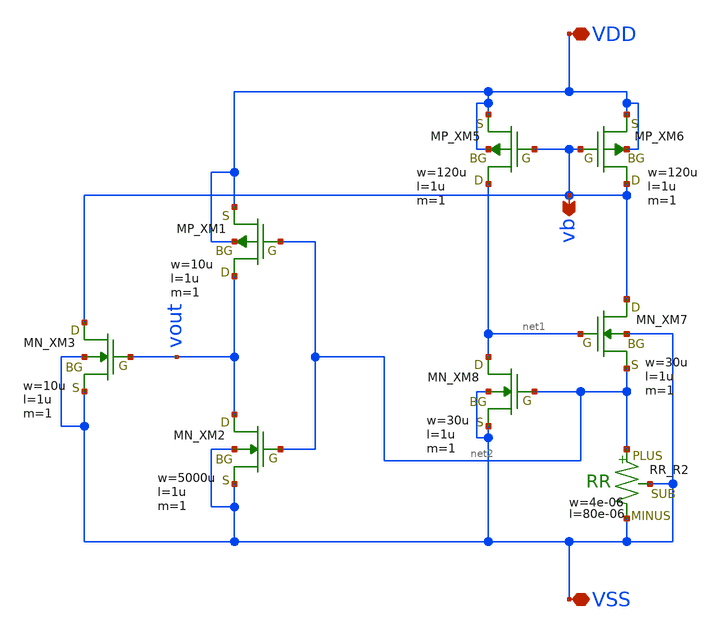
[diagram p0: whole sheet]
** sch_path: TR10/current-source/cs_startup_usage.sch
**.subckt cs_startup_usage VDD VSS vb
*.iopin VDD
*.iopin VSS
*.opin vb
XM5 net1 vb VDD VDD PMOS w=120u l=1u as=0 ad=0 ps=0 pd=0 nrd=0 nrs=0 m=1
XM6 vb vb VDD VDD PMOS w=120u l=1u as=0 ad=0 ps=0 pd=0 nrd=0 nrs=0 m=1
XM7 vb net1 net2 VSS NMOS w=30u l=1u as=0 ad=0 ps=0 pd=0 nrd=0 nrs=0 m=1
XM8 net1 net2 VSS VSS NMOS w=30u l=1u as=0 ad=0 ps=0 pd=0 nrd=0 nrs=0 m=1
XR2 net2 VSS VSS F_RR w=4e-06 R=1 l=80e-06 tc1=0 tc2=0
XM1 vout net2 VDD VDD PMOS w=10u l=1u as=0 ad=0 ps=0 pd=0 nrd=0 nrs=0 m=1
XM2 vout net2 VSS VSS NMOS w=5000u l=1u as=0 ad=0 ps=0 pd=0 nrd=0 nrs=0 m=1
XM3 vb vout VSS VSS NMOS w=10u l=1u as=0 ad=0 ps=0 pd=0 nrd=0 nrs=0 m=1
**.ends
.end
